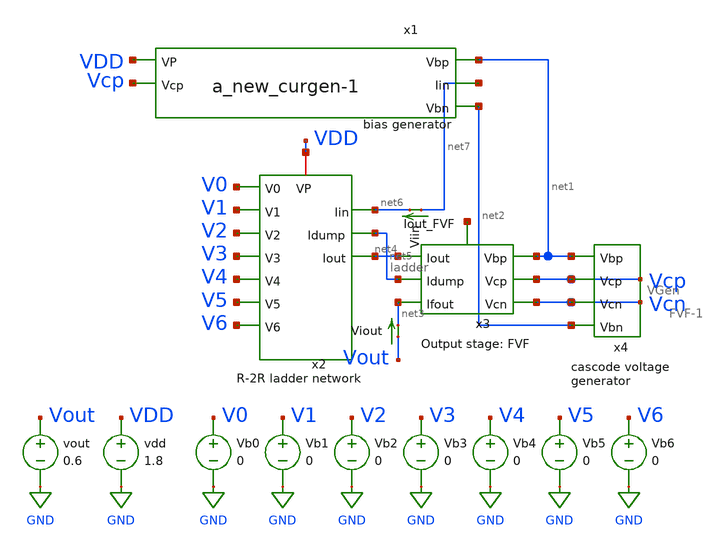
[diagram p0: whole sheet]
** sch_path: xschem/new_sim_cascode.sch
**.subckt new_sim_cascode
Vb1 V1 GND 0
Vb2 V2 GND 0
Vb3 V3 GND 0
Vb4 V4 GND 0
Vb5 V5 GND 0
Vb6 V6 GND 0
Vb0 V0 GND 0
x3 net1 Vcp net4 Vcn net3 net5 net8 FVF-1
x4 net1 Vcn Vcp net2 VGen
vdd VDD GND 1.8
vout Vout GND 0.6
Viout Vout net3 0
.save i(viout)
Viin net7 net6 0
.save i(viin)
x2 V0 VDD net5 net4 net6 V1 V2 V3 V4 V5 V6 ladder
x1 VDD net1 Vcp net7 net2 a_new_curgen-1
**** begin user architecture code

.option wnflag=1
.param MC_SWITCH=1.0
.lib ~/skywater/skywater-pdk/libraries/sky130_fd_pr_ngspice/latest/models/sky130.lib.spice tt



.control
  set wr_singlescale
let runs = 10
  let run = 1
	while run <= runs
 set appendwrite = FALSE
  set wr_vecnames
  let code = 0
  while code < 128
    if code eq 0
      let b0 = 0
    else
      let b0 = code % 2
    end
    if floor(code / 2) eq 0
      let b1 = 0
    else
      let b1 = floor(code / 2) % 2
    end
    if floor(code / 4) eq 0
      let b2 = 0
    else
      let b2 = floor(code / 4) % 2
    end
    if floor(code / 8) eq 0
      let b3 = 0
    else
      let b3 = floor(code / 8) % 2
    end
    if floor(code / 16) eq 0
      let b4 = 0
    else
      let b4 = floor(code / 16) % 2
    end
    if floor(code / 32) eq 0
      let b5 = 0
    else
      let b5 = floor(code / 32) % 2
    end
    if floor(code / 64) eq 0
      let b6 = 0
    else
      let b6 = floor(code / 64) % 2
    end
    alter Vb0 1.8*$&b0
    alter Vb1 1.8*$&b1
    alter Vb2 1.8*$&b2
    alter Vb3 1.8*$&b3
    alter Vb4 1.8*$&b4
    alter Vb5 1.8*$&b5
    alter Vb6 1.8*$&b6
    save all
    op
    wrdata ~/new_24_12/new_24_12_{$&run}.txt v(b0) v(b1) v(b2) v(b3) v(b4) v(b5) v(b6) v(Vout) i(Viout)
    if code eq 0
      set appendwrite
      set wr_vecnames = FALSE
    end
    let code = code + 1
  end
reset
let run = run + 1
end
  quit
.endc

**** end user architecture code
**.ends

* expanding   symbol:  ./FVF-1.sym # of pins=7
** sym_path: xschem/old_files/FVF-1.sym
** sch_path: xschem/old_files/FVF-1.sch
.subckt FVF-1 Vbp Vcp Iout Vcn Ifout Idump Iout_FVF
*.ipin Vcn
*.ipin Iout
*.ipin Idump
*.ipin Vcp
*.ipin Vbp
*.opin Ifout
*.opin Iout_FVF
XM1 net1 Vcn Idump GND sky130_fd_pr__nfet_01v8 L=8 W=24 nf=1 ad='int((nf+1)/2) * W/nf * 0.29' as='int((nf+2)/2) * W/nf * 0.29'
+ pd='2*int((nf+1)/2) * (W/nf + 0.29)' ps='2*int((nf+2)/2) * (W/nf + 0.29)' nrd='0.29 / W' nrs='0.29 / W'
+ sa=0 sb=0 sd=0 mult=1 m=1
XM2 GND net1 Idump GND sky130_fd_pr__nfet_01v8 L=8 W=24 nf=1 ad='int((nf+1)/2) * W/nf * 0.29' as='int((nf+2)/2) * W/nf * 0.29'
+ pd='2*int((nf+1)/2) * (W/nf + 0.29)' ps='2*int((nf+2)/2) * (W/nf + 0.29)' nrd='0.29 / W' nrs='0.29 / W'
+ sa=0 sb=0 sd=0 mult=1 m=1
XM3 Iout_FVF Vcn Iout GND sky130_fd_pr__nfet_01v8 L=8 W=24 nf=1 ad='int((nf+1)/2) * W/nf * 0.29' as='int((nf+2)/2) * W/nf * 0.29'
+ pd='2*int((nf+1)/2) * (W/nf + 0.29)' ps='2*int((nf+2)/2) * (W/nf + 0.29)' nrd='0.29 / W' nrs='0.29 / W'
+ sa=0 sb=0 sd=0 mult=1 m=1
XM4 GND Iout_FVF Iout GND sky130_fd_pr__nfet_01v8 L=8 W=24 nf=1 ad='int((nf+1)/2) * W/nf * 0.29' as='int((nf+2)/2) * W/nf * 0.29'
+ pd='2*int((nf+1)/2) * (W/nf + 0.29)' ps='2*int((nf+2)/2) * (W/nf + 0.29)' nrd='0.29 / W' nrs='0.29 / W'
+ sa=0 sb=0 sd=0 mult=1 m=1
XM5 Ifout Vcn net2 GND sky130_fd_pr__nfet_01v8 L=8 W=24 nf=1 ad='int((nf+1)/2) * W/nf * 0.29' as='int((nf+2)/2) * W/nf * 0.29'
+ pd='2*int((nf+1)/2) * (W/nf + 0.29)' ps='2*int((nf+2)/2) * (W/nf + 0.29)' nrd='0.29 / W' nrs='0.29 / W'
+ sa=0 sb=0 sd=0 mult=1 m=1
XM6 net2 Iout_FVF GND GND sky130_fd_pr__nfet_01v8 L=8 W=24 nf=1 ad='int((nf+1)/2) * W/nf * 0.29' as='int((nf+2)/2) * W/nf * 0.29'
+ pd='2*int((nf+1)/2) * (W/nf + 0.29)' ps='2*int((nf+2)/2) * (W/nf + 0.29)' nrd='0.29 / W' nrs='0.29 / W'
+ sa=0 sb=0 sd=0 mult=1 m=1
XM7 net1 Vcp net3 VDD sky130_fd_pr__pfet_01v8 L=8 W=24 nf=1 ad='int((nf+1)/2) * W/nf * 0.29' as='int((nf+2)/2) * W/nf * 0.29'
+ pd='2*int((nf+1)/2) * (W/nf + 0.29)' ps='2*int((nf+2)/2) * (W/nf + 0.29)' nrd='0.29 / W' nrs='0.29 / W'
+ sa=0 sb=0 sd=0 mult=1 m=1
XM8 Iout_FVF Vcp net4 VDD sky130_fd_pr__pfet_01v8 L=8 W=24 nf=1 ad='int((nf+1)/2) * W/nf * 0.29' as='int((nf+2)/2) * W/nf * 0.29'
+ pd='2*int((nf+1)/2) * (W/nf + 0.29)' ps='2*int((nf+2)/2) * (W/nf + 0.29)' nrd='0.29 / W' nrs='0.29 / W'
+ sa=0 sb=0 sd=0 mult=1 m=1
XM9 Ifout Vcp net5 VDD sky130_fd_pr__pfet_01v8 L=8 W=24 nf=1 ad='int((nf+1)/2) * W/nf * 0.29' as='int((nf+2)/2) * W/nf * 0.29'
+ pd='2*int((nf+1)/2) * (W/nf + 0.29)' ps='2*int((nf+2)/2) * (W/nf + 0.29)' nrd='0.29 / W' nrs='0.29 / W'
+ sa=0 sb=0 sd=0 mult=1 m=1
XM15 net3 Vbp VDD VDD sky130_fd_pr__pfet_01v8 L=8 W=24 nf=1 ad='int((nf+1)/2) * W/nf * 0.29' as='int((nf+2)/2) * W/nf * 0.29'
+ pd='2*int((nf+1)/2) * (W/nf + 0.29)' ps='2*int((nf+2)/2) * (W/nf + 0.29)' nrd='0.29 / W' nrs='0.29 / W'
+ sa=0 sb=0 sd=0 mult=1 m=1
XM16 net4 Vbp VDD VDD sky130_fd_pr__pfet_01v8 L=8 W=24 nf=1 ad='int((nf+1)/2) * W/nf * 0.29' as='int((nf+2)/2) * W/nf * 0.29'
+ pd='2*int((nf+1)/2) * (W/nf + 0.29)' ps='2*int((nf+2)/2) * (W/nf + 0.29)' nrd='0.29 / W' nrs='0.29 / W'
+ sa=0 sb=0 sd=0 mult=1 m=1
XM17 net5 Vbp VDD VDD sky130_fd_pr__pfet_01v8 L=8 W=24 nf=1 ad='int((nf+1)/2) * W/nf * 0.29' as='int((nf+2)/2) * W/nf * 0.29'
+ pd='2*int((nf+1)/2) * (W/nf + 0.29)' ps='2*int((nf+2)/2) * (W/nf + 0.29)' nrd='0.29 / W' nrs='0.29 / W'
+ sa=0 sb=0 sd=0 mult=1 m=1
.ends


* expanding   symbol:  ./VGen.sym # of pins=4
** sym_path: xschem/VGen.sym
** sch_path: xschem/VGen.sch
.subckt VGen Vbp Vcn Vcp Vbn
*.opin Vcp
*.ipin Vbp
*.ipin Vbn
*.opin Vcn
XM5 net4 net4 net1 GND sky130_fd_pr__nfet_01v8 L=12 W=96 nf=1 ad='int((nf+1)/2) * W/nf * 0.29' as='int((nf+2)/2) * W/nf * 0.29'
+ pd='2*int((nf+1)/2) * (W/nf + 0.29)' ps='2*int((nf+2)/2) * (W/nf + 0.29)' nrd='0.29 / W' nrs='0.29 / W'
+ sa=0 sb=0 sd=0 mult=1 m=1
XM6 net1 net4 GND GND sky130_fd_pr__nfet_01v8 L=12 W=24 nf=1 ad='int((nf+1)/2) * W/nf * 0.29' as='int((nf+2)/2) * W/nf * 0.29'
+ pd='2*int((nf+1)/2) * (W/nf + 0.29)' ps='2*int((nf+2)/2) * (W/nf + 0.29)' nrd='0.29 / W' nrs='0.29 / W'
+ sa=0 sb=0 sd=0 mult=1 m=1
XM4 net1 Vcn Vcn GND sky130_fd_pr__nfet_01v8 L=12 W=24 nf=1 ad='int((nf+1)/2) * W/nf * 0.29' as='int((nf+2)/2) * W/nf * 0.29'
+ pd='2*int((nf+1)/2) * (W/nf + 0.29)' ps='2*int((nf+2)/2) * (W/nf + 0.29)' nrd='0.29 / W' nrs='0.29 / W'
+ sa=0 sb=0 sd=0 mult=1 m=1
XM1 VDD Vbp net4 VDD sky130_fd_pr__pfet_01v8 L=48 W=24 nf=1 ad='int((nf+1)/2) * W/nf * 0.29' as='int((nf+2)/2) * W/nf * 0.29'
+ pd='2*int((nf+1)/2) * (W/nf + 0.29)' ps='2*int((nf+2)/2) * (W/nf + 0.29)' nrd='0.29 / W' nrs='0.29 / W'
+ sa=0 sb=0 sd=0 mult=1 m=1
XM2 VDD Vbp Vcn VDD sky130_fd_pr__pfet_01v8 L=12 W=24 nf=1 ad='int((nf+1)/2) * W/nf * 0.29' as='int((nf+2)/2) * W/nf * 0.29'
+ pd='2*int((nf+1)/2) * (W/nf + 0.29)' ps='2*int((nf+2)/2) * (W/nf + 0.29)' nrd='0.29 / W' nrs='0.29 / W'
+ sa=0 sb=0 sd=0 mult=1 m=1
XM9 net3 net3 net2 VDD sky130_fd_pr__pfet_01v8 L=12 W=96 nf=1 ad='int((nf+1)/2) * W/nf * 0.29' as='int((nf+2)/2) * W/nf * 0.29'
+ pd='2*int((nf+1)/2) * (W/nf + 0.29)' ps='2*int((nf+2)/2) * (W/nf + 0.29)' nrd='0.29 / W' nrs='0.29 / W'
+ sa=0 sb=0 sd=0 mult=1 m=1
XM11 GND Vbn Vcp GND sky130_fd_pr__nfet_01v8 L=12 W=24 nf=1 ad='int((nf+1)/2) * W/nf * 0.29' as='int((nf+2)/2) * W/nf * 0.29'
+ pd='2*int((nf+1)/2) * (W/nf + 0.29)' ps='2*int((nf+2)/2) * (W/nf + 0.29)' nrd='0.29 / W' nrs='0.29 / W'
+ sa=0 sb=0 sd=0 mult=1 m=1
XM8 net2 Vcp Vcp VDD sky130_fd_pr__pfet_01v8 L=12 W=24 nf=1 ad='int((nf+1)/2) * W/nf * 0.29' as='int((nf+2)/2) * W/nf * 0.29'
+ pd='2*int((nf+1)/2) * (W/nf + 0.29)' ps='2*int((nf+2)/2) * (W/nf + 0.29)' nrd='0.29 / W' nrs='0.29 / W'
+ sa=0 sb=0 sd=0 mult=1 m=1
XM12 GND Vbn net3 GND sky130_fd_pr__nfet_01v8 L=48 W=24 nf=1 ad='int((nf+1)/2) * W/nf * 0.29' as='int((nf+2)/2) * W/nf * 0.29'
+ pd='2*int((nf+1)/2) * (W/nf + 0.29)' ps='2*int((nf+2)/2) * (W/nf + 0.29)' nrd='0.29 / W' nrs='0.29 / W'
+ sa=0 sb=0 sd=0 mult=1 m=1
XM7 net2 net3 VDD VDD sky130_fd_pr__pfet_01v8 L=12 W=24 nf=1 ad='int((nf+1)/2) * W/nf * 0.29' as='int((nf+2)/2) * W/nf * 0.29'
+ pd='2*int((nf+1)/2) * (W/nf + 0.29)' ps='2*int((nf+2)/2) * (W/nf + 0.29)' nrd='0.29 / W' nrs='0.29 / W'
+ sa=0 sb=0 sd=0 mult=1 m=1
.ends


* expanding   symbol:  ./ladder.sym # of pins=11
** sym_path: ./ladder.sym
** sch_path: ./ladder.sch
.subckt ladder V0 VP Idump Iout Iin V1 V2 V3 V4 V5 V6
*.ipin V6
*.ipin V5
*.ipin V4
*.ipin V3
*.ipin V2
*.ipin V1
*.ipin V0
*.iopin VP
*.iopin Iin
*.opin Idump
*.opin Iout
XM1 Iin VP net1 GND sky130_fd_pr__nfet_01v8 L=4 W=12 nf=1 ad='int((nf+1)/2) * W/nf * 0.29' as='int((nf+2)/2) * W/nf * 0.29'
+ pd='2*int((nf+1)/2) * (W/nf + 0.29)' ps='2*int((nf+2)/2) * (W/nf + 0.29)' nrd='0.29 / W' nrs='0.29 / W'
+ sa=0 sb=0 sd=0 mult=1 m=1
XM3 Iin VP net2 GND sky130_fd_pr__nfet_01v8 L=4 W=12 nf=1 ad='int((nf+1)/2) * W/nf * 0.29' as='int((nf+2)/2) * W/nf * 0.29'
+ pd='2*int((nf+1)/2) * (W/nf + 0.29)' ps='2*int((nf+2)/2) * (W/nf + 0.29)' nrd='0.29 / W' nrs='0.29 / W'
+ sa=0 sb=0 sd=0 mult=1 m=1
XM5 net2 VP net3 GND sky130_fd_pr__nfet_01v8 L=4 W=12 nf=1 ad='int((nf+1)/2) * W/nf * 0.29' as='int((nf+2)/2) * W/nf * 0.29'
+ pd='2*int((nf+1)/2) * (W/nf + 0.29)' ps='2*int((nf+2)/2) * (W/nf + 0.29)' nrd='0.29 / W' nrs='0.29 / W'
+ sa=0 sb=0 sd=0 mult=1 m=1
XM7 net2 VP net4 GND sky130_fd_pr__nfet_01v8 L=4 W=12 nf=1 ad='int((nf+1)/2) * W/nf * 0.29' as='int((nf+2)/2) * W/nf * 0.29'
+ pd='2*int((nf+1)/2) * (W/nf + 0.29)' ps='2*int((nf+2)/2) * (W/nf + 0.29)' nrd='0.29 / W' nrs='0.29 / W'
+ sa=0 sb=0 sd=0 mult=1 m=1
XM6 net3 V5 Iout GND sky130_fd_pr__nfet_01v8 L=4 W=12 nf=1 ad='int((nf+1)/2) * W/nf * 0.29' as='int((nf+2)/2) * W/nf * 0.29'
+ pd='2*int((nf+1)/2) * (W/nf + 0.29)' ps='2*int((nf+2)/2) * (W/nf + 0.29)' nrd='0.29 / W' nrs='0.29 / W'
+ sa=0 sb=0 sd=0 mult=1 m=1
XM8 net3 net16 Idump GND sky130_fd_pr__nfet_01v8 L=4 W=12 nf=1 ad='int((nf+1)/2) * W/nf * 0.29' as='int((nf+2)/2) * W/nf * 0.29'
+ pd='2*int((nf+1)/2) * (W/nf + 0.29)' ps='2*int((nf+2)/2) * (W/nf + 0.29)' nrd='0.29 / W' nrs='0.29 / W'
+ sa=0 sb=0 sd=0 mult=1 m=1
XM2 net1 V6 Iout GND sky130_fd_pr__nfet_01v8 L=4 W=12 nf=1 ad='int((nf+1)/2) * W/nf * 0.29' as='int((nf+2)/2) * W/nf * 0.29'
+ pd='2*int((nf+1)/2) * (W/nf + 0.29)' ps='2*int((nf+2)/2) * (W/nf + 0.29)' nrd='0.29 / W' nrs='0.29 / W'
+ sa=0 sb=0 sd=0 mult=1 m=1
XM4 net1 net15 Idump GND sky130_fd_pr__nfet_01v8 L=4 W=12 nf=1 ad='int((nf+1)/2) * W/nf * 0.29' as='int((nf+2)/2) * W/nf * 0.29'
+ pd='2*int((nf+1)/2) * (W/nf + 0.29)' ps='2*int((nf+2)/2) * (W/nf + 0.29)' nrd='0.29 / W' nrs='0.29 / W'
+ sa=0 sb=0 sd=0 mult=1 m=1
XM9 net4 VP net5 GND sky130_fd_pr__nfet_01v8 L=4 W=12 nf=1 ad='int((nf+1)/2) * W/nf * 0.29' as='int((nf+2)/2) * W/nf * 0.29'
+ pd='2*int((nf+1)/2) * (W/nf + 0.29)' ps='2*int((nf+2)/2) * (W/nf + 0.29)' nrd='0.29 / W' nrs='0.29 / W'
+ sa=0 sb=0 sd=0 mult=1 m=1
XM11 net4 VP net6 GND sky130_fd_pr__nfet_01v8 L=4 W=12 nf=1 ad='int((nf+1)/2) * W/nf * 0.29' as='int((nf+2)/2) * W/nf * 0.29'
+ pd='2*int((nf+1)/2) * (W/nf + 0.29)' ps='2*int((nf+2)/2) * (W/nf + 0.29)' nrd='0.29 / W' nrs='0.29 / W'
+ sa=0 sb=0 sd=0 mult=1 m=1
XM10 net5 V4 Iout GND sky130_fd_pr__nfet_01v8 L=4 W=12 nf=1 ad='int((nf+1)/2) * W/nf * 0.29' as='int((nf+2)/2) * W/nf * 0.29'
+ pd='2*int((nf+1)/2) * (W/nf + 0.29)' ps='2*int((nf+2)/2) * (W/nf + 0.29)' nrd='0.29 / W' nrs='0.29 / W'
+ sa=0 sb=0 sd=0 mult=1 m=1
XM12 net5 net17 Idump GND sky130_fd_pr__nfet_01v8 L=4 W=12 nf=1 ad='int((nf+1)/2) * W/nf * 0.29' as='int((nf+2)/2) * W/nf * 0.29'
+ pd='2*int((nf+1)/2) * (W/nf + 0.29)' ps='2*int((nf+2)/2) * (W/nf + 0.29)' nrd='0.29 / W' nrs='0.29 / W'
+ sa=0 sb=0 sd=0 mult=1 m=1
XM13 net6 VP net7 GND sky130_fd_pr__nfet_01v8 L=4 W=12 nf=1 ad='int((nf+1)/2) * W/nf * 0.29' as='int((nf+2)/2) * W/nf * 0.29'
+ pd='2*int((nf+1)/2) * (W/nf + 0.29)' ps='2*int((nf+2)/2) * (W/nf + 0.29)' nrd='0.29 / W' nrs='0.29 / W'
+ sa=0 sb=0 sd=0 mult=1 m=1
XM15 net6 VP net8 GND sky130_fd_pr__nfet_01v8 L=4 W=12 nf=1 ad='int((nf+1)/2) * W/nf * 0.29' as='int((nf+2)/2) * W/nf * 0.29'
+ pd='2*int((nf+1)/2) * (W/nf + 0.29)' ps='2*int((nf+2)/2) * (W/nf + 0.29)' nrd='0.29 / W' nrs='0.29 / W'
+ sa=0 sb=0 sd=0 mult=1 m=1
XM14 net7 V3 Iout GND sky130_fd_pr__nfet_01v8 L=4 W=12 nf=1 ad='int((nf+1)/2) * W/nf * 0.29' as='int((nf+2)/2) * W/nf * 0.29'
+ pd='2*int((nf+1)/2) * (W/nf + 0.29)' ps='2*int((nf+2)/2) * (W/nf + 0.29)' nrd='0.29 / W' nrs='0.29 / W'
+ sa=0 sb=0 sd=0 mult=1 m=1
XM16 net7 net18 Idump GND sky130_fd_pr__nfet_01v8 L=4 W=12 nf=1 ad='int((nf+1)/2) * W/nf * 0.29' as='int((nf+2)/2) * W/nf * 0.29'
+ pd='2*int((nf+1)/2) * (W/nf + 0.29)' ps='2*int((nf+2)/2) * (W/nf + 0.29)' nrd='0.29 / W' nrs='0.29 / W'
+ sa=0 sb=0 sd=0 mult=1 m=1
XM17 net8 VP net9 GND sky130_fd_pr__nfet_01v8 L=4 W=12 nf=1 ad='int((nf+1)/2) * W/nf * 0.29' as='int((nf+2)/2) * W/nf * 0.29'
+ pd='2*int((nf+1)/2) * (W/nf + 0.29)' ps='2*int((nf+2)/2) * (W/nf + 0.29)' nrd='0.29 / W' nrs='0.29 / W'
+ sa=0 sb=0 sd=0 mult=1 m=1
XM19 net8 VP net10 GND sky130_fd_pr__nfet_01v8 L=4 W=12 nf=1 ad='int((nf+1)/2) * W/nf * 0.29' as='int((nf+2)/2) * W/nf * 0.29'
+ pd='2*int((nf+1)/2) * (W/nf + 0.29)' ps='2*int((nf+2)/2) * (W/nf + 0.29)' nrd='0.29 / W' nrs='0.29 / W'
+ sa=0 sb=0 sd=0 mult=1 m=1
XM18 net9 V2 Iout GND sky130_fd_pr__nfet_01v8 L=4 W=12 nf=1 ad='int((nf+1)/2) * W/nf * 0.29' as='int((nf+2)/2) * W/nf * 0.29'
+ pd='2*int((nf+1)/2) * (W/nf + 0.29)' ps='2*int((nf+2)/2) * (W/nf + 0.29)' nrd='0.29 / W' nrs='0.29 / W'
+ sa=0 sb=0 sd=0 mult=1 m=1
XM20 net9 net19 Idump GND sky130_fd_pr__nfet_01v8 L=4 W=12 nf=1 ad='int((nf+1)/2) * W/nf * 0.29' as='int((nf+2)/2) * W/nf * 0.29'
+ pd='2*int((nf+1)/2) * (W/nf + 0.29)' ps='2*int((nf+2)/2) * (W/nf + 0.29)' nrd='0.29 / W' nrs='0.29 / W'
+ sa=0 sb=0 sd=0 mult=1 m=1
XM21 net10 VP net11 GND sky130_fd_pr__nfet_01v8 L=4 W=12 nf=1 ad='int((nf+1)/2) * W/nf * 0.29' as='int((nf+2)/2) * W/nf * 0.29'
+ pd='2*int((nf+1)/2) * (W/nf + 0.29)' ps='2*int((nf+2)/2) * (W/nf + 0.29)' nrd='0.29 / W' nrs='0.29 / W'
+ sa=0 sb=0 sd=0 mult=1 m=1
XM23 net10 VP net12 GND sky130_fd_pr__nfet_01v8 L=4 W=12 nf=1 ad='int((nf+1)/2) * W/nf * 0.29' as='int((nf+2)/2) * W/nf * 0.29'
+ pd='2*int((nf+1)/2) * (W/nf + 0.29)' ps='2*int((nf+2)/2) * (W/nf + 0.29)' nrd='0.29 / W' nrs='0.29 / W'
+ sa=0 sb=0 sd=0 mult=1 m=1
XM22 net11 V1 Iout GND sky130_fd_pr__nfet_01v8 L=4 W=12 nf=1 ad='int((nf+1)/2) * W/nf * 0.29' as='int((nf+2)/2) * W/nf * 0.29'
+ pd='2*int((nf+1)/2) * (W/nf + 0.29)' ps='2*int((nf+2)/2) * (W/nf + 0.29)' nrd='0.29 / W' nrs='0.29 / W'
+ sa=0 sb=0 sd=0 mult=1 m=1
XM24 net11 net20 Idump GND sky130_fd_pr__nfet_01v8 L=4 W=12 nf=1 ad='int((nf+1)/2) * W/nf * 0.29' as='int((nf+2)/2) * W/nf * 0.29'
+ pd='2*int((nf+1)/2) * (W/nf + 0.29)' ps='2*int((nf+2)/2) * (W/nf + 0.29)' nrd='0.29 / W' nrs='0.29 / W'
+ sa=0 sb=0 sd=0 mult=1 m=1
XM25 net12 VP net13 GND sky130_fd_pr__nfet_01v8 L=4 W=12 nf=1 ad='int((nf+1)/2) * W/nf * 0.29' as='int((nf+2)/2) * W/nf * 0.29'
+ pd='2*int((nf+1)/2) * (W/nf + 0.29)' ps='2*int((nf+2)/2) * (W/nf + 0.29)' nrd='0.29 / W' nrs='0.29 / W'
+ sa=0 sb=0 sd=0 mult=1 m=1
XM27 net12 VP net14 GND sky130_fd_pr__nfet_01v8 L=4 W=12 nf=1 ad='int((nf+1)/2) * W/nf * 0.29' as='int((nf+2)/2) * W/nf * 0.29'
+ pd='2*int((nf+1)/2) * (W/nf + 0.29)' ps='2*int((nf+2)/2) * (W/nf + 0.29)' nrd='0.29 / W' nrs='0.29 / W'
+ sa=0 sb=0 sd=0 mult=1 m=1
XM26 net13 V0 Iout GND sky130_fd_pr__nfet_01v8 L=4 W=12 nf=1 ad='int((nf+1)/2) * W/nf * 0.29' as='int((nf+2)/2) * W/nf * 0.29'
+ pd='2*int((nf+1)/2) * (W/nf + 0.29)' ps='2*int((nf+2)/2) * (W/nf + 0.29)' nrd='0.29 / W' nrs='0.29 / W'
+ sa=0 sb=0 sd=0 mult=1 m=1
XM28 net13 net21 Idump GND sky130_fd_pr__nfet_01v8 L=4 W=12 nf=1 ad='int((nf+1)/2) * W/nf * 0.29' as='int((nf+2)/2) * W/nf * 0.29'
+ pd='2*int((nf+1)/2) * (W/nf + 0.29)' ps='2*int((nf+2)/2) * (W/nf + 0.29)' nrd='0.29 / W' nrs='0.29 / W'
+ sa=0 sb=0 sd=0 mult=1 m=1
XM29 net14 VP Idump GND sky130_fd_pr__nfet_01v8 L=4 W=12 nf=1 ad='int((nf+1)/2) * W/nf * 0.29' as='int((nf+2)/2) * W/nf * 0.29'
+ pd='2*int((nf+1)/2) * (W/nf + 0.29)' ps='2*int((nf+2)/2) * (W/nf + 0.29)' nrd='0.29 / W' nrs='0.29 / W'
+ sa=0 sb=0 sd=0 mult=1 m=1
x1 net15 V6 inverter
x2 net16 V5 inverter
x3 net17 V4 inverter
x4 net18 V3 inverter
x5 net19 V2 inverter
x6 net20 V1 inverter
x7 net21 V0 inverter
.ends


* expanding   symbol:  /home/madvlsi/Documents/MP4/DAC-VLSI/xschem/a_new_curgen-1.sym # of pins=5
** sym_path: xschem/old_files/a_new_curgen-1.sym
** sch_path: xschem/old_files/a_new_curgen-1.sch
.subckt a_new_curgen-1 VP Vbp Vcp Iin Vbn
*.opin Iin
*.ipin VP
*.opin Vbp
*.opin Vbn
*.ipin Vcp
XM1 Vbn Vbn GND GND sky130_fd_pr__nfet_01v8 L=8 W=24 nf=1 ad='int((nf+1)/2) * W/nf * 0.29' as='int((nf+2)/2) * W/nf * 0.29'
+ pd='2*int((nf+1)/2) * (W/nf + 0.29)' ps='2*int((nf+2)/2) * (W/nf + 0.29)' nrd='0.29 / W' nrs='0.29 / W'
+ sa=0 sb=0 sd=0 mult=1 m=1
XM2 GND Vbn Vbp GND sky130_fd_pr__nfet_01v8 L=8 W=24 nf=1 ad='int((nf+1)/2) * W/nf * 0.29' as='int((nf+2)/2) * W/nf * 0.29'
+ pd='2*int((nf+1)/2) * (W/nf + 0.29)' ps='2*int((nf+2)/2) * (W/nf + 0.29)' nrd='0.29 / W' nrs='0.29 / W'
+ sa=0 sb=0 sd=0 mult=1 m=1
XM3 net1 net2 GND GND sky130_fd_pr__nfet_01v8 L=8 W=24 nf=1 ad='int((nf+1)/2) * W/nf * 0.29' as='int((nf+2)/2) * W/nf * 0.29'
+ pd='2*int((nf+1)/2) * (W/nf + 0.29)' ps='2*int((nf+2)/2) * (W/nf + 0.29)' nrd='0.29 / W' nrs='0.29 / W'
+ sa=0 sb=0 sd=0 mult=1 m=1
XM4 net7 net2 net2 GND sky130_fd_pr__nfet_01v8 L=8 W=24 nf=1 ad='int((nf+1)/2) * W/nf * 0.29' as='int((nf+2)/2) * W/nf * 0.29'
+ pd='2*int((nf+1)/2) * (W/nf + 0.29)' ps='2*int((nf+2)/2) * (W/nf + 0.29)' nrd='0.29 / W' nrs='0.29 / W'
+ sa=0 sb=0 sd=0 mult=8 m=8
XM7 net3 Vcp net2 VDD sky130_fd_pr__pfet_01v8 L=8 W=24 nf=1 ad='int((nf+1)/2) * W/nf * 0.29' as='int((nf+2)/2) * W/nf * 0.29'
+ pd='2*int((nf+1)/2) * (W/nf + 0.29)' ps='2*int((nf+2)/2) * (W/nf + 0.29)' nrd='0.29 / W' nrs='0.29 / W'
+ sa=0 sb=0 sd=0 mult=1 m=1
XM8 Vbn Vcp net4 VDD sky130_fd_pr__pfet_01v8 L=8 W=24 nf=1 ad='int((nf+1)/2) * W/nf * 0.29' as='int((nf+2)/2) * W/nf * 0.29'
+ pd='2*int((nf+1)/2) * (W/nf + 0.29)' ps='2*int((nf+2)/2) * (W/nf + 0.29)' nrd='0.29 / W' nrs='0.29 / W'
+ sa=0 sb=0 sd=0 mult=1 m=1
R1 net7 GND 90K m=1
XM9 Iin Vcp net6 VDD sky130_fd_pr__pfet_01v8 L=8 W=24 nf=1 ad='int((nf+1)/2) * W/nf * 0.29' as='int((nf+2)/2) * W/nf * 0.29'
+ pd='2*int((nf+1)/2) * (W/nf + 0.29)' ps='2*int((nf+2)/2) * (W/nf + 0.29)' nrd='0.29 / W' nrs='0.29 / W'
+ sa=0 sb=0 sd=0 mult=1 m=1
XM10 VP Vbp net3 VDD sky130_fd_pr__pfet_01v8 L=8 W=24 nf=1 ad='int((nf+1)/2) * W/nf * 0.29' as='int((nf+2)/2) * W/nf * 0.29'
+ pd='2*int((nf+1)/2) * (W/nf + 0.29)' ps='2*int((nf+2)/2) * (W/nf + 0.29)' nrd='0.29 / W' nrs='0.29 / W'
+ sa=0 sb=0 sd=0 mult=1 m=1
XM11 VP net5 net5 VDD sky130_fd_pr__pfet_01v8 L=8 W=24 nf=1 ad='int((nf+1)/2) * W/nf * 0.29' as='int((nf+2)/2) * W/nf * 0.29'
+ pd='2*int((nf+1)/2) * (W/nf + 0.29)' ps='2*int((nf+2)/2) * (W/nf + 0.29)' nrd='0.29 / W' nrs='0.29 / W'
+ sa=0 sb=0 sd=0 mult=1 m=1
XM12 VP net5 Vbp VDD sky130_fd_pr__pfet_01v8 L=8 W=24 nf=1 ad='int((nf+1)/2) * W/nf * 0.29' as='int((nf+2)/2) * W/nf * 0.29'
+ pd='2*int((nf+1)/2) * (W/nf + 0.29)' ps='2*int((nf+2)/2) * (W/nf + 0.29)' nrd='0.29 / W' nrs='0.29 / W'
+ sa=0 sb=0 sd=0 mult=1 m=1
XM13 VP Vbp net4 VDD sky130_fd_pr__pfet_01v8 L=8 W=24 nf=1 ad='int((nf+1)/2) * W/nf * 0.29' as='int((nf+2)/2) * W/nf * 0.29'
+ pd='2*int((nf+1)/2) * (W/nf + 0.29)' ps='2*int((nf+2)/2) * (W/nf + 0.29)' nrd='0.29 / W' nrs='0.29 / W'
+ sa=0 sb=0 sd=0 mult=1 m=1
XM14 VP Vbp net6 VDD sky130_fd_pr__pfet_01v8 L=8 W=24 nf=1 ad='int((nf+1)/2) * W/nf * 0.29' as='int((nf+2)/2) * W/nf * 0.29'
+ pd='2*int((nf+1)/2) * (W/nf + 0.29)' ps='2*int((nf+2)/2) * (W/nf + 0.29)' nrd='0.29 / W' nrs='0.29 / W'
+ sa=0 sb=0 sd=0 mult=1 m=1
XM5 net1 Vcp net5 VDD sky130_fd_pr__pfet_01v8 L=8 W=24 nf=1 ad='int((nf+1)/2) * W/nf * 0.29' as='int((nf+2)/2) * W/nf * 0.29'
+ pd='2*int((nf+1)/2) * (W/nf + 0.29)' ps='2*int((nf+2)/2) * (W/nf + 0.29)' nrd='0.29 / W' nrs='0.29 / W'
+ sa=0 sb=0 sd=0 mult=1 m=1
.ends


* expanding   symbol:  ./inverter.sym # of pins=2
** sym_path: xschem/inverter.sym
** sch_path: xschem/inverter.sch
.subckt inverter Y A
*.ipin A
*.opin Y
XM1 Y A VDD VDD sky130_fd_pr__pfet_01v8 L=0.15 W=1 nf=1 ad='int((nf+1)/2) * W/nf * 0.29' as='int((nf+2)/2) * W/nf * 0.29'
+ pd='2*int((nf+1)/2) * (W/nf + 0.29)' ps='2*int((nf+2)/2) * (W/nf + 0.29)' nrd='0.29 / W' nrs='0.29 / W'
+ sa=0 sb=0 sd=0 mult=1 m=1
XM2 Y A GND GND sky130_fd_pr__nfet_01v8 L=0.15 W=1 nf=1 ad='int((nf+1)/2) * W/nf * 0.29' as='int((nf+2)/2) * W/nf * 0.29'
+ pd='2*int((nf+1)/2) * (W/nf + 0.29)' ps='2*int((nf+2)/2) * (W/nf + 0.29)' nrd='0.29 / W' nrs='0.29 / W'
+ sa=0 sb=0 sd=0 mult=1 m=1
.ends

.GLOBAL GND
.GLOBAL VDD
.end
